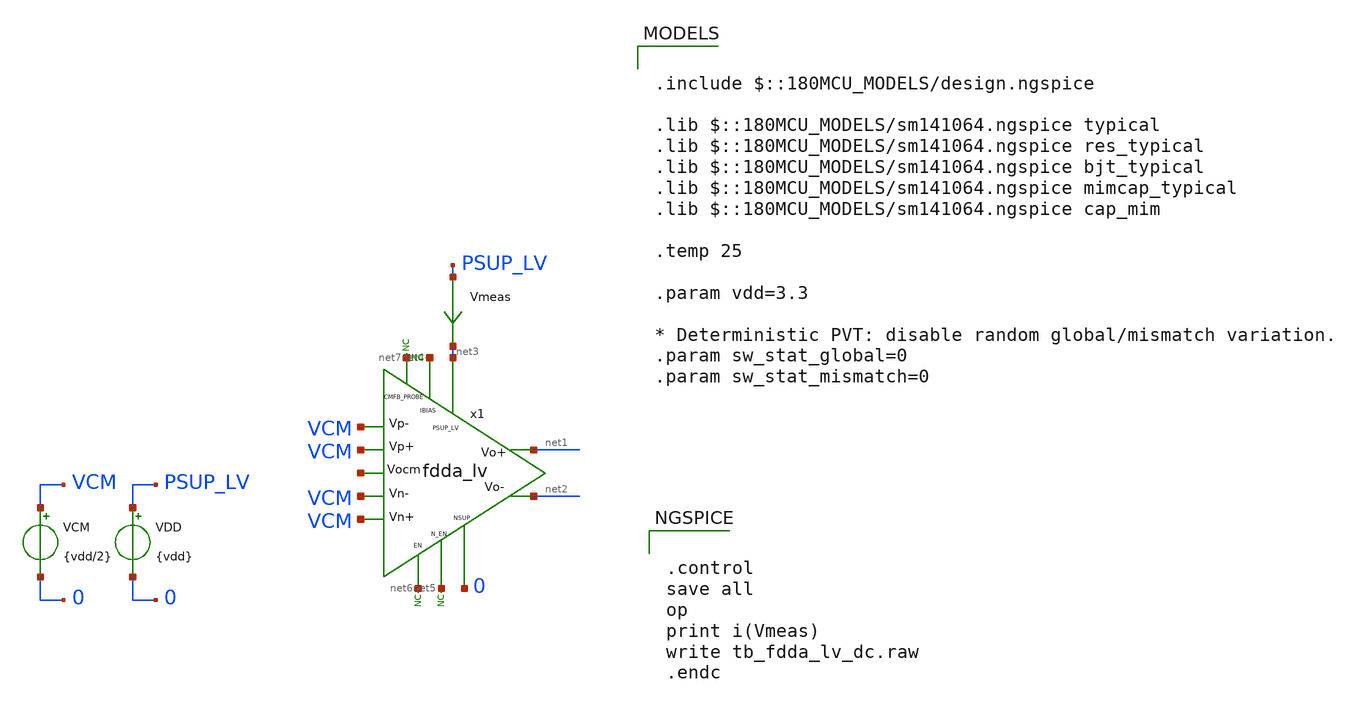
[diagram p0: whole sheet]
** sch_path: xschem/blocks/fdda_lv/tb_fdda_lv_dc.sch
**.subckt tb_fdda_lv_dc
x1 net3 VCM VCM VCM VCM net1 net2 net4 net5 net6 0 net7 net8 fdda_lv
* noconn #net4
* noconn #net7
* noconn #net6
* noconn #net5
VDD PSUP_LV 0 {vdd}
VCM VCM 0 {vdd/2}
Vmeas PSUP_LV net3 0
.save i(vmeas)
**** begin user architecture code


.control
save all
op
print i(Vmeas)
write tb_fdda_lv_dc.raw
.endc



.include $::180MCU_MODELS/design.ngspice

.lib $::180MCU_MODELS/sm141064.ngspice typical
.lib $::180MCU_MODELS/sm141064.ngspice res_typical
.lib $::180MCU_MODELS/sm141064.ngspice bjt_typical
.lib $::180MCU_MODELS/sm141064.ngspice mimcap_typical
.lib $::180MCU_MODELS/sm141064.ngspice cap_mim

.temp 25

.param vdd=3.3

* Deterministic PVT: disable random global/mismatch variation.
.param sw_stat_global=0
.param sw_stat_mismatch=0


**** end user architecture code
**.ends
.end
